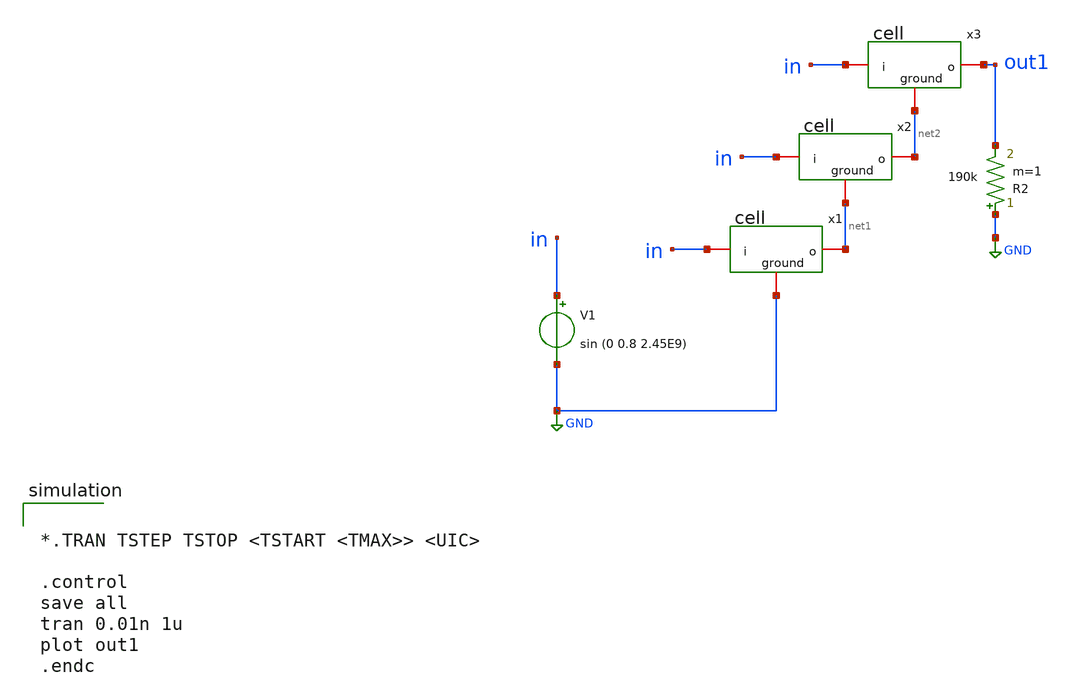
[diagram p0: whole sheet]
** sch_path: xschem/matching/multiplier-full-3.sch
**.subckt multiplier-full-3
V1 in GND sin (0 0.8 2.45E9)
x1 net1 in GND cell
x2 net2 in net1 cell
R2 GND out1 190k m=1
x3 out1 in net2 cell
**** begin user architecture code


*.TRAN TSTEP TSTOP <TSTART <TMAX>> <UIC>

.control
save all
tran 0.01n 1u
plot out1
.endc



** opencircuitdesign pdks install
.lib $::SKYWATER_MODELS/sky130.lib.spice tt


**** end user architecture code
**.ends

* expanding   symbol:  cell.sym # of pins=3
** sym_path: xschem/cell.sym
** sch_path: xschem/cell.sch
.subckt cell o i ground
*.iopin ground
*.iopin o
*.iopin i
XM10 net1 net1 ground net1 sky130_fd_pr__pfet_01v8_lvt L=0.35 W=40 nf=5 ad='int((5 + 1)/2) * 40 / 5 * 0.29'
+ as='int((5 + 2)/2) * 40 / 5 * 0.29' pd='2*int((5 + 1)/2) * (40 / 5 + 0.29)' ps='2*int((5 + 2)/2) * (40 / 5 + 0.29)'
+ nrd='0.29 / 40 ' nrs='0.29 / 40 ' sa=0 sb=0 sd=0 mult=1 m=1
XM1 o o net1 o sky130_fd_pr__pfet_01v8_lvt L=0.35 W=40 nf=5 ad='int((5 + 1)/2) * 40 / 5 * 0.29' as='int((5 + 2)/2) * 40 / 5 * 0.29'
+ pd='2*int((5 + 1)/2) * (40 / 5 + 0.29)' ps='2*int((5 + 2)/2) * (40 / 5 + 0.29)' nrd='0.29 / 40 ' nrs='0.29 / 40 '
+ sa=0 sb=0 sd=0 mult=1 m=1
XC3 o ground sky130_fd_pr__cap_mim_m3_1 W=30 L=30 MF=3 m=3
XC2 net1 i sky130_fd_pr__cap_mim_m3_1 W=30 L=30 MF=1 m=1
.ends

.GLOBAL GND
.end
